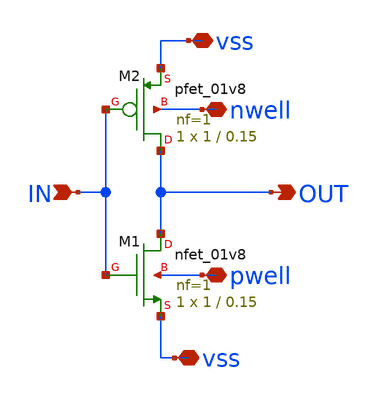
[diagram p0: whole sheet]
** sch_path: design/core/sqar_inv_b/sqar_inv_b.sch
**.subckt sqar_inv_b IN OUT nwell pwell vss vss
*.ipin IN
*.opin OUT
*.iopin nwell
*.iopin pwell
*.iopin vss
*.iopin vss
XM1 OUT IN vss pwell sky130_fd_pr__nfet_01v8 L=0.15 W=1 nf=1 ad='int((nf+1)/2) * W/nf * 0.29' as='int((nf+2)/2) * W/nf * 0.29'
+ pd='2*int((nf+1)/2) * (W/nf + 0.29)' ps='2*int((nf+2)/2) * (W/nf + 0.29)' nrd='0.29 / W' nrs='0.29 / W'
+ sa=0 sb=0 sd=0 mult=1 m=1
XM2 OUT IN vss nwell sky130_fd_pr__pfet_01v8 L=0.15 W=1 nf=1 ad='int((nf+1)/2) * W/nf * 0.29' as='int((nf+2)/2) * W/nf * 0.29'
+ pd='2*int((nf+1)/2) * (W/nf + 0.29)' ps='2*int((nf+2)/2) * (W/nf + 0.29)' nrd='0.29 / W' nrs='0.29 / W'
+ sa=0 sb=0 sd=0 mult=1 m=1
**.ends
.end
